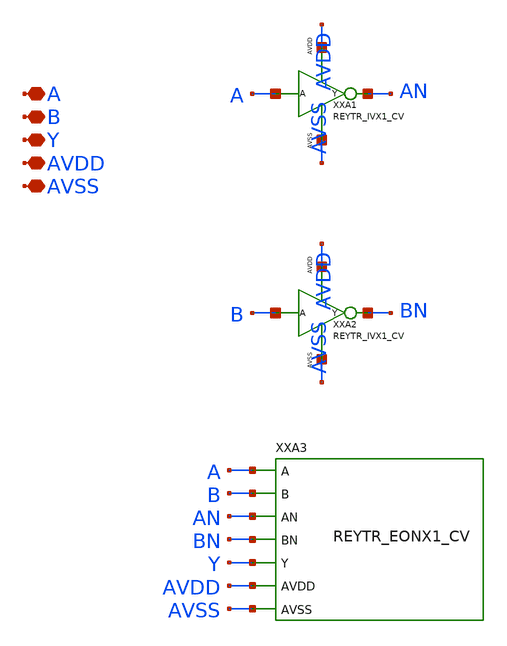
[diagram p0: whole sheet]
** sch_path: design/REY_TR_SKY130A/REYTR_EOX1_CV.sch
**.subckt REYTR_EOX1_CV A B Y AVDD AVSS
*.iopin A
*.iopin B
*.iopin Y
*.iopin AVDD
*.iopin AVSS
XXA1 A AN AVDD AVSS REYTR_IVX1_CV
XXA2 B BN AVDD AVSS REYTR_IVX1_CV
XXA3 A B AN BN Y AVDD AVSS REYTR_EONX1_CV
**.ends
.end
